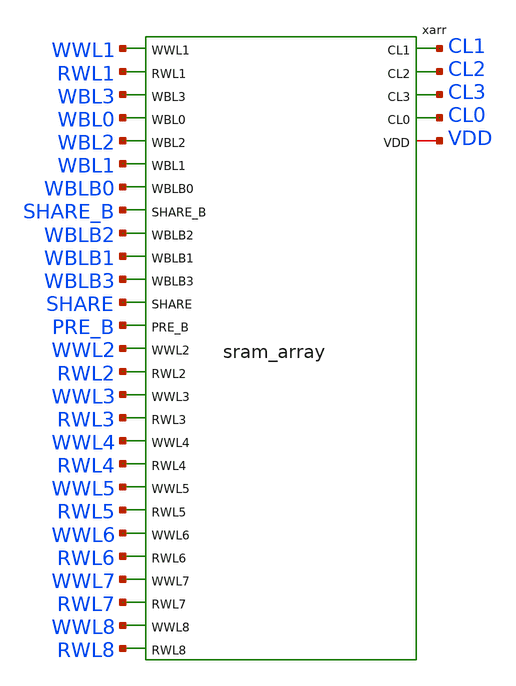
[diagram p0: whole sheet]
** sch_path: schematics/sram4x8.sch
**.subckt sram4x8
xarr CL1 CL2 CL3 WWL1 CL0 RWL1 WBL3 WBL0 WBL2 WBL1 VDD WBLB0 SHARE_B WBLB2 WBLB1 WBLB3 SHARE PRE_B
+ WWL2 RWL2 WWL3 RWL3 WWL4 RWL4 WWL5 RWL5 WWL6 RWL6 WWL7 RWL7 WWL8 RWL8 sram_array
**** begin user architecture code


.lib /usr/local/share/pdk/sky130A/libs.tech/ngspice/sky130.lib.spice ss

.param vdd_v=1.8
.param tmp=27
.temp {tmp}
.param csig=0
.param td=0.5e-9
.param ts={10.5e-9+td}
.param pat=255
.param in1={floor(pat/1)-2*floor(pat/2)} in2={floor(pat/2)-2*floor(pat/4)}
.param in3={floor(pat/4)-2*floor(pat/8)} in4={floor(pat/8)-2*floor(pat/16)}
.param in5={floor(pat/16)-2*floor(pat/32)} in6={floor(pat/32)-2*floor(pat/64)}
.param in7={floor(pat/64)-2*floor(pat/128)} in8={floor(pat/128)-2*floor(pat/256)}

* weights w<row><col>, rows 1-8, cols 0-3
.param w10=1 w20=1 w30=1 w40=1 w50=1 w60=1 w70=1 w80=1
.param w11=1 w21=1 w31=1 w41=1 w51=0 w61=0 w71=0 w81=0
.param w12=1 w22=0 w32=1 w42=0 w52=1 w62=0 w72=1 w82=0
.param w13=0 w23=1 w33=1 w43=1 w53=1 w63=1 w73=0 w83=0

.ic v(xarr.xc0.x1.q)={w10*vdd_v} v(xarr.xc0.x1.qb)={(1-w10)*vdd_v}
.ic v(xarr.xc0.x2.q)={w20*vdd_v} v(xarr.xc0.x2.qb)={(1-w20)*vdd_v}
.ic v(xarr.xc0.x3.q)={w30*vdd_v} v(xarr.xc0.x3.qb)={(1-w30)*vdd_v}
.ic v(xarr.xc0.x4.q)={w40*vdd_v} v(xarr.xc0.x4.qb)={(1-w40)*vdd_v}
.ic v(xarr.xc0.x5.q)={w50*vdd_v} v(xarr.xc0.x5.qb)={(1-w50)*vdd_v}
.ic v(xarr.xc0.x6.q)={w60*vdd_v} v(xarr.xc0.x6.qb)={(1-w60)*vdd_v}
.ic v(xarr.xc0.x7.q)={w70*vdd_v} v(xarr.xc0.x7.qb)={(1-w70)*vdd_v}
.ic v(xarr.xc0.x8.q)={w80*vdd_v} v(xarr.xc0.x8.qb)={(1-w80)*vdd_v}
.ic v(xarr.xc1.x1.q)={w11*vdd_v} v(xarr.xc1.x1.qb)={(1-w11)*vdd_v}
.ic v(xarr.xc1.x2.q)={w21*vdd_v} v(xarr.xc1.x2.qb)={(1-w21)*vdd_v}
.ic v(xarr.xc1.x3.q)={w31*vdd_v} v(xarr.xc1.x3.qb)={(1-w31)*vdd_v}
.ic v(xarr.xc1.x4.q)={w41*vdd_v} v(xarr.xc1.x4.qb)={(1-w41)*vdd_v}
.ic v(xarr.xc1.x5.q)={w51*vdd_v} v(xarr.xc1.x5.qb)={(1-w51)*vdd_v}
.ic v(xarr.xc1.x6.q)={w61*vdd_v} v(xarr.xc1.x6.qb)={(1-w61)*vdd_v}
.ic v(xarr.xc1.x7.q)={w71*vdd_v} v(xarr.xc1.x7.qb)={(1-w71)*vdd_v}
.ic v(xarr.xc1.x8.q)={w81*vdd_v} v(xarr.xc1.x8.qb)={(1-w81)*vdd_v}
.ic v(xarr.xc2.x1.q)={w12*vdd_v} v(xarr.xc2.x1.qb)={(1-w12)*vdd_v}
.ic v(xarr.xc2.x2.q)={w22*vdd_v} v(xarr.xc2.x2.qb)={(1-w22)*vdd_v}
.ic v(xarr.xc2.x3.q)={w32*vdd_v} v(xarr.xc2.x3.qb)={(1-w32)*vdd_v}
.ic v(xarr.xc2.x4.q)={w42*vdd_v} v(xarr.xc2.x4.qb)={(1-w42)*vdd_v}
.ic v(xarr.xc2.x5.q)={w52*vdd_v} v(xarr.xc2.x5.qb)={(1-w52)*vdd_v}
.ic v(xarr.xc2.x6.q)={w62*vdd_v} v(xarr.xc2.x6.qb)={(1-w62)*vdd_v}
.ic v(xarr.xc2.x7.q)={w72*vdd_v} v(xarr.xc2.x7.qb)={(1-w72)*vdd_v}
.ic v(xarr.xc2.x8.q)={w82*vdd_v} v(xarr.xc2.x8.qb)={(1-w82)*vdd_v}
.ic v(xarr.xc3.x1.q)={w13*vdd_v} v(xarr.xc3.x1.qb)={(1-w13)*vdd_v}
.ic v(xarr.xc3.x2.q)={w23*vdd_v} v(xarr.xc3.x2.qb)={(1-w23)*vdd_v}
.ic v(xarr.xc3.x3.q)={w33*vdd_v} v(xarr.xc3.x3.qb)={(1-w33)*vdd_v}
.ic v(xarr.xc3.x4.q)={w43*vdd_v} v(xarr.xc3.x4.qb)={(1-w43)*vdd_v}
.ic v(xarr.xc3.x5.q)={w53*vdd_v} v(xarr.xc3.x5.qb)={(1-w53)*vdd_v}
.ic v(xarr.xc3.x6.q)={w63*vdd_v} v(xarr.xc3.x6.qb)={(1-w63)*vdd_v}
.ic v(xarr.xc3.x7.q)={w73*vdd_v} v(xarr.xc3.x7.qb)={(1-w73)*vdd_v}
.ic v(xarr.xc3.x8.q)={w83*vdd_v} v(xarr.xc3.x8.qb)={(1-w83)*vdd_v}

Vsup VDD 0 {vdd_v}
Vwbl0 WBL0 0 0
Vwblb0 WBLB0 0 0
Vwbl1 WBL1 0 0
Vwblb1 WBLB1 0 0
Vwbl2 WBL2 0 0
Vwblb2 WBLB2 0 0
Vwbl3 WBL3 0 0
Vwblb3 WBLB3 0 0
Vww1 WWL1 0 0
Vww2 WWL2 0 0
Vww3 WWL3 0 0
Vww4 WWL4 0 0
Vww5 WWL5 0 0
Vww6 WWL6 0 0
Vww7 WWL7 0 0
Vww8 WWL8 0 0

Vpre PRE_B 0 PWL(0 0 9.9n 0 10n {vdd_v})
Vsh SHARE 0 PWL(0 {vdd_v} 9.9n {vdd_v} 10n 0 {ts-0.1e-9} 0 {ts} {vdd_v})
Vshb SHARE_B 0 PWL(0 0 9.9n 0 10n {vdd_v} {ts-0.1e-9} {vdd_v} {ts} 0)

Vr1 RWL1 0 PWL(0 0 10.1n 0 10.2n {in1*vdd_v} {10.2e-9+td} {in1*vdd_v} {10.3e-9+td} 0)
Vr2 RWL2 0 PWL(0 0 10.1n 0 10.2n {in2*vdd_v} {10.2e-9+td} {in2*vdd_v} {10.3e-9+td} 0)
Vr3 RWL3 0 PWL(0 0 10.1n 0 10.2n {in3*vdd_v} {10.2e-9+td} {in3*vdd_v} {10.3e-9+td} 0)
Vr4 RWL4 0 PWL(0 0 10.1n 0 10.2n {in4*vdd_v} {10.2e-9+td} {in4*vdd_v} {10.3e-9+td} 0)
Vr5 RWL5 0 PWL(0 0 10.1n 0 10.2n {in5*vdd_v} {10.2e-9+td} {in5*vdd_v} {10.3e-9+td} 0)
Vr6 RWL6 0 PWL(0 0 10.1n 0 10.2n {in6*vdd_v} {10.2e-9+td} {in6*vdd_v} {10.3e-9+td} 0)
Vr7 RWL7 0 PWL(0 0 10.1n 0 10.2n {in7*vdd_v} {10.2e-9+td} {in7*vdd_v} {10.3e-9+td} 0)
Vr8 RWL8 0 PWL(0 0 10.1n 0 10.2n {in8*vdd_v} {10.2e-9+td} {in8*vdd_v} {10.3e-9+td} 0)

.tran 0.02n 16n uic
.save v(CL0) v(CL1) v(CL2) v(CL3)

.control
set cname = ss
foreach vv 1.62 1.8 1.98
  foreach tv -40 27 125
    foreach pv 255 173 0 170 85 15 240 1 127 118 201 60
      alterparam vdd_v=$vv
      alterparam tmp=$tv
      alterparam pat=$pv
      reset
      run
      meas tran c0 find v(cl0) at=13n
      meas tran c1 find v(cl1) at=13n
      meas tran c2 find v(cl2) at=13n
      meas tran c3 find v(cl3) at=13n
      echo $cname $vv $tv $pv $&c0 $&c1 $&c2 $&c3 >> array_pvt.csv
    end
  end
end
.endc

**** end user architecture code
**.ends
.end
